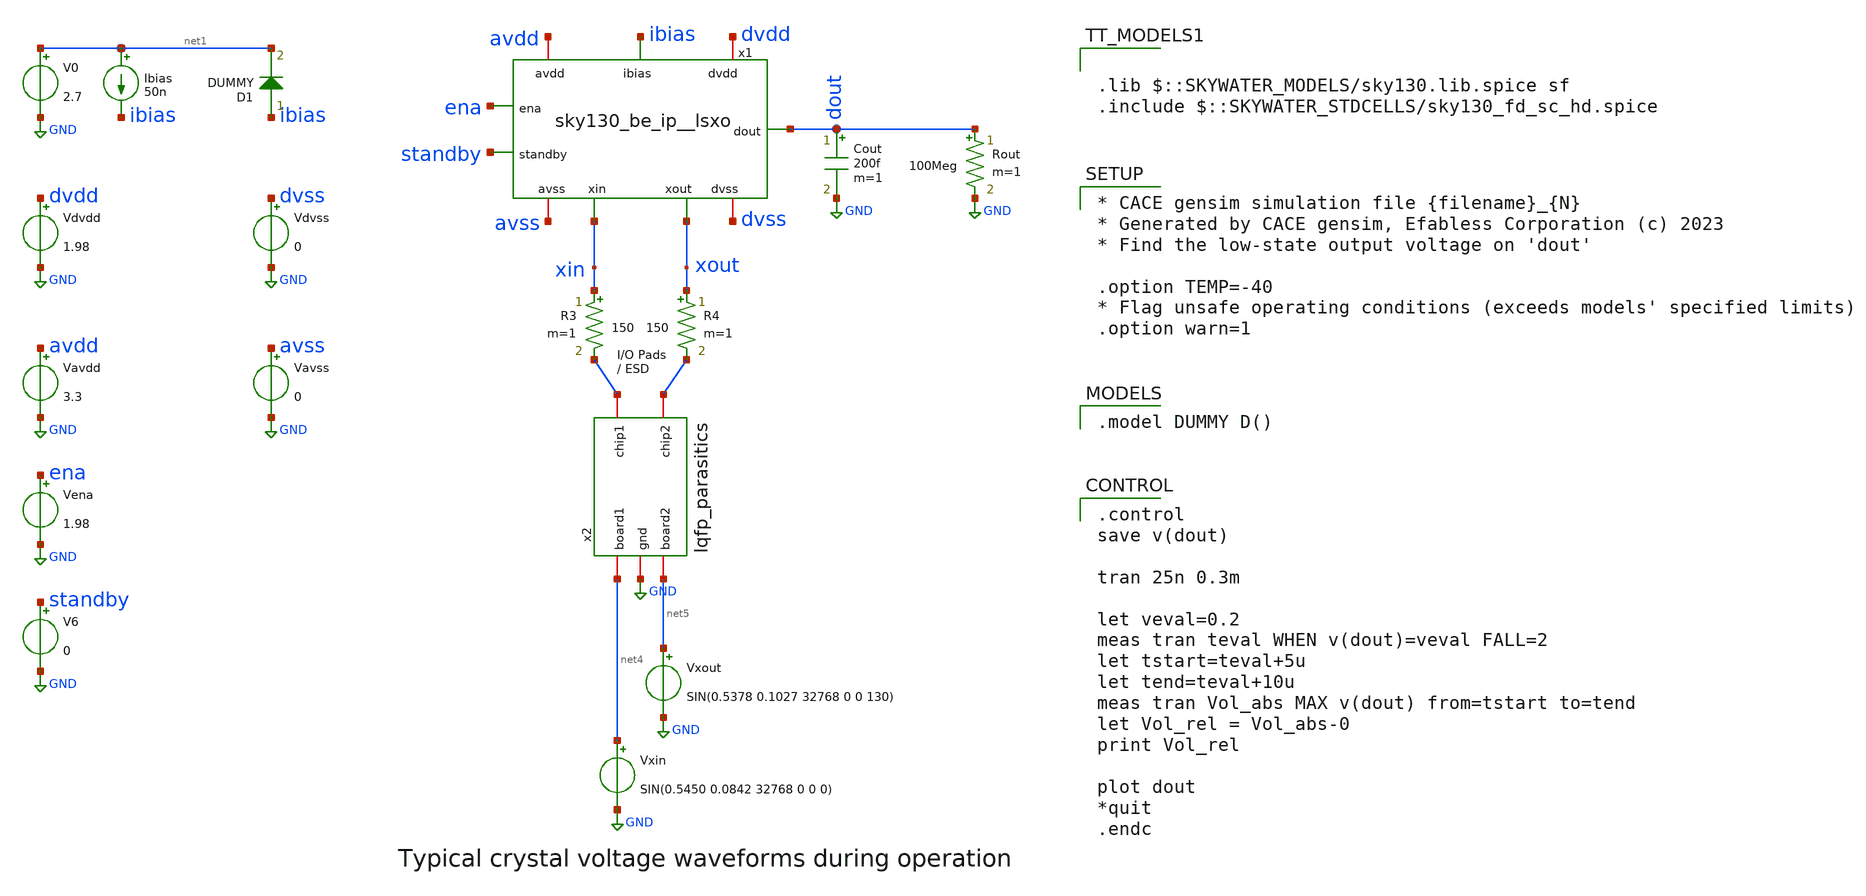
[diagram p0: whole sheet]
** sch_path: xschem/tb_man__vol.sch

.lib $::SKYWATER_MODELS/sky130.lib.spice sf
.include $::SKYWATER_STDCELLS/sky130_fd_sc_hd.spice

**.subckt tb_man__vol
Vdvdd dvdd GND 1.98
Vavdd avdd GND 3.3
Ibias net1 ibias 50n
Cout dout GND 200f m=1
V0 net1 GND 2.7
V6 standby GND 0
R3 xin net2 150 m=1
R4 xout net3 150 m=1
x2 net3 net2 GND net4 net5 lqfp_parasitics
Vena ena GND 1.98
D1 ibias net1 DUMMY area=100
x1 avdd avss dvdd dvss ibias ena standby dout xin xout sky130_be_ip__lsxo
Vdvss dvss GND 0
Vavss avss GND 0
Rout dout GND 100Meg m=1
Vxout net5 GND SIN(0.5378 0.1027 32768 0 0 130)
Vxin net4 GND SIN(0.5450 0.0842 32768 0 0 0)
**** begin user architecture code

.model DUMMY D()


.control
save v(dout)

tran 25n 0.3m

let veval=0.2
meas tran teval WHEN v(dout)=veval FALL=2
let tstart=teval+5u
let tend=teval+10u
meas tran Vol_abs MAX v(dout) from=tstart to=tend
let Vol_rel = Vol_abs-0
print Vol_rel

plot dout
*quit
.endc



* CACE gensim simulation file {filename}_{N}
* Generated by CACE gensim, Efabless Corporation (c) 2023
* Find the low-state output voltage on 'dout'

.option TEMP=-40
* Flag unsafe operating conditions (exceeds models' specified limits)
.option warn=1


**** end user architecture code
**.ends
.GLOBAL GND
.end
